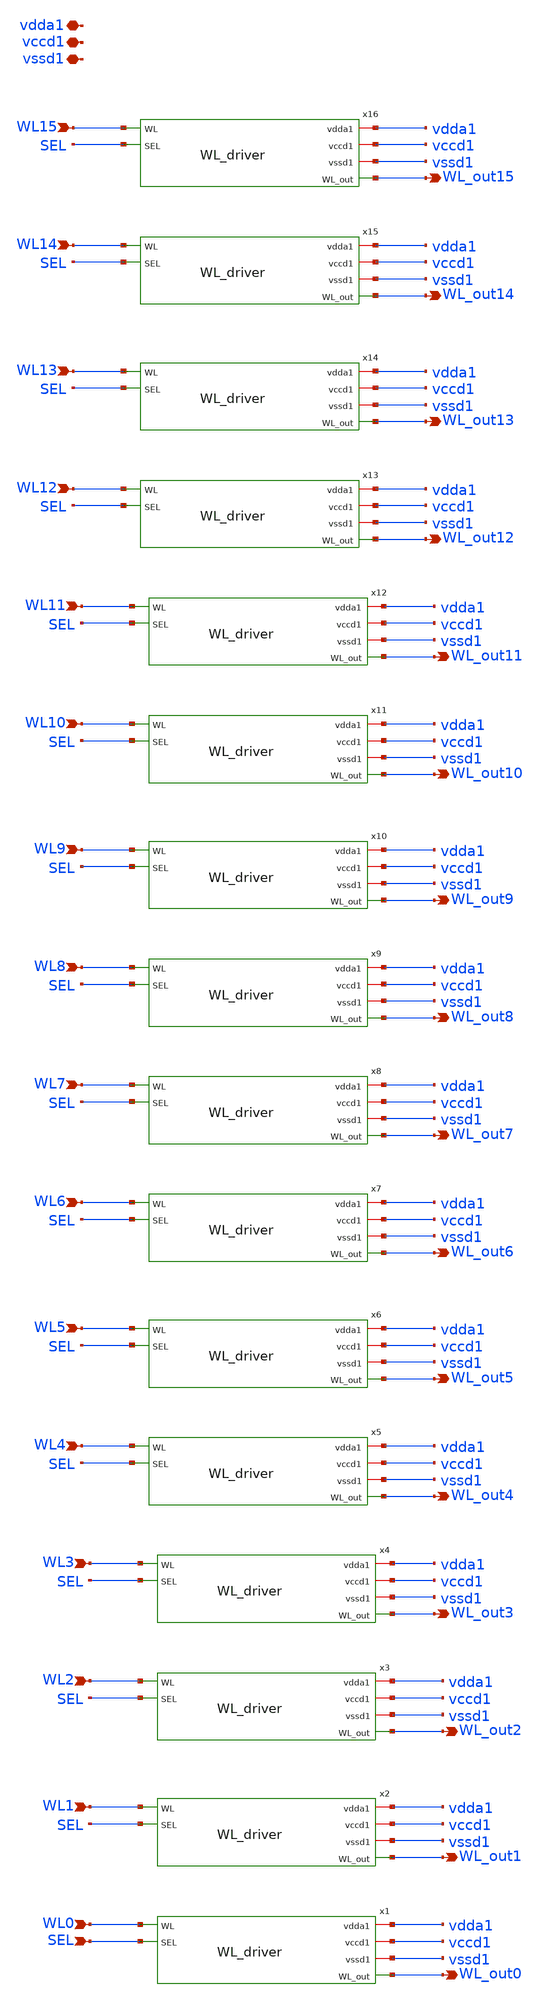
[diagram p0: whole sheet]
** sch_path: xschem/WL_drivers_16x1.sch
**.subckt WL_drivers_16x1 WL0 SEL vdda1 vccd1 vssd1 WL_out0 WL_out1 WL2 WL_out2 WL1 WL_out3 WL4
*+ WL_out4 WL3 WL5 WL_out5 WL6 WL_out6 WL7 WL_out7 WL8 WL_out8 WL9 WL_out9 WL10 WL_out10 WL11 WL_out11 WL12
*+ WL_out12 WL13 WL_out13 WL14 WL_out14 WL15 WL_out15
*.ipin WL0
*.ipin SEL
*.iopin vdda1
*.iopin vccd1
*.iopin vssd1
*.opin WL_out0
*.opin WL_out1
*.ipin WL2
*.opin WL_out2
*.ipin WL1
*.opin WL_out3
*.ipin WL4
*.opin WL_out4
*.ipin WL3
*.ipin WL5
*.opin WL_out5
*.ipin WL6
*.opin WL_out6
*.ipin WL7
*.opin WL_out7
*.ipin WL8
*.opin WL_out8
*.ipin WL9
*.opin WL_out9
*.ipin WL10
*.opin WL_out10
*.ipin WL11
*.opin WL_out11
*.ipin WL12
*.opin WL_out12
*.ipin WL13
*.opin WL_out13
*.ipin WL14
*.opin WL_out14
*.ipin WL15
*.opin WL_out15
x1 vdda1 vccd1 vssd1 WL0 SEL WL_out0 WL_driver
x2 vdda1 vccd1 vssd1 WL1 SEL WL_out1 WL_driver
x3 vdda1 vccd1 vssd1 WL2 SEL WL_out2 WL_driver
x4 vdda1 vccd1 vssd1 WL3 SEL WL_out3 WL_driver
x5 vdda1 vccd1 vssd1 WL4 SEL WL_out4 WL_driver
x6 vdda1 vccd1 vssd1 WL5 SEL WL_out5 WL_driver
x7 vdda1 vccd1 vssd1 WL6 SEL WL_out6 WL_driver
x8 vdda1 vccd1 vssd1 WL7 SEL WL_out7 WL_driver
x9 vdda1 vccd1 vssd1 WL8 SEL WL_out8 WL_driver
x10 vdda1 vccd1 vssd1 WL9 SEL WL_out9 WL_driver
x11 vdda1 vccd1 vssd1 WL10 SEL WL_out10 WL_driver
x12 vdda1 vccd1 vssd1 WL11 SEL WL_out11 WL_driver
x13 vdda1 vccd1 vssd1 WL12 SEL WL_out12 WL_driver
x14 vdda1 vccd1 vssd1 WL13 SEL WL_out13 WL_driver
x15 vdda1 vccd1 vssd1 WL14 SEL WL_out14 WL_driver
x16 vdda1 vccd1 vssd1 WL15 SEL WL_out15 WL_driver
**.ends
.end
